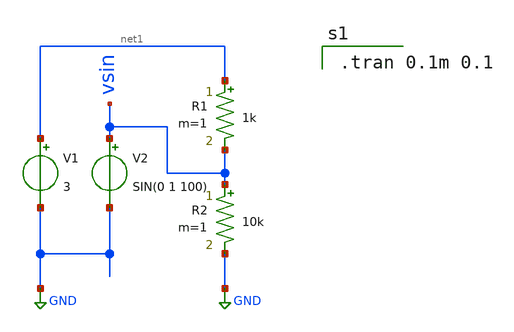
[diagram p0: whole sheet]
** sch_path: XSCHEM_SCHEMATICS/TEST_SIM_1/T1_sim_01.sch
**.subckt T1_sim_01
V1 net1 GND 3
R1 net1 vsin 1k m=1
R2 vsin GND 10k m=1
V2 vsin GND SIN(0 1 100)
**** begin user architecture code

.tran 0.1m 0.1

**** end user architecture code
**.ends
.GLOBAL GND
.end
